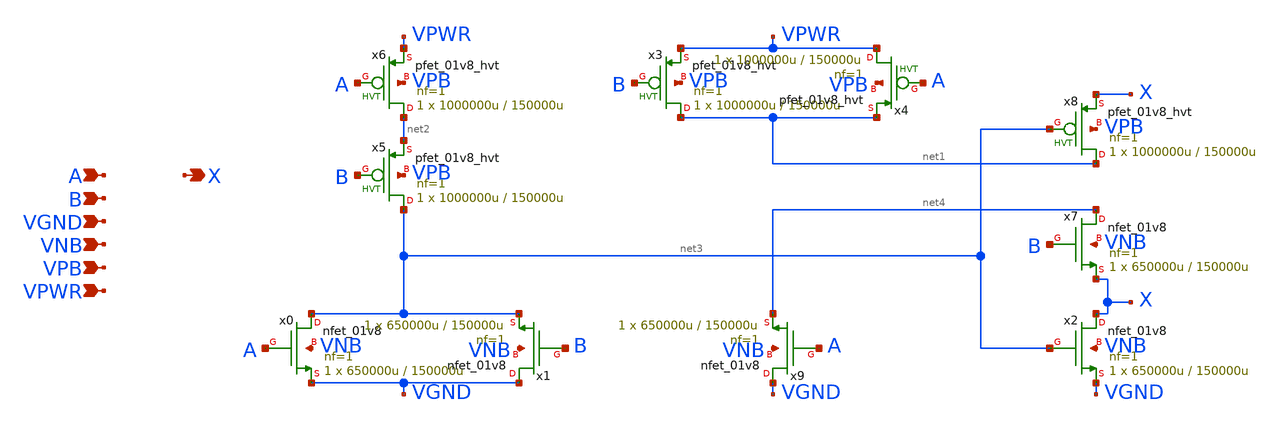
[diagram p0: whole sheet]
** sch_path: schematics/xor2/sky130_fd_sc_hd__xor2_1.sch
**.subckt sky130_fd_sc_hd__xor2_1 A X B VGND VNB VPB VPWR
*.ipin A
*.opin X
*.ipin B
*.ipin VGND
*.ipin VNB
*.ipin VPB
*.ipin VPWR
Xx3 net1 B VPWR VPB sky130_fd_pr__pfet_01v8_hvt L=150000u W=1000000u nf=1 ad='int((1 + 1)/2) * 1000000u / 1 * 0.29'
+ as='int((1 + 2)/2) * 1000000u / 1 * 0.29' pd='2*int((1 + 1)/2) * (1000000u / 1 + 0.29)' ps='2*int((1 + 2)/2) * (1000000u / 1 + 0.29)'
+ nrd='0.29 / 1000000u ' nrs='0.29 / 1000000u ' sa=0 sb=0 sd=0 mult=1 m=1
Xx4 VPWR A net1 VPB sky130_fd_pr__pfet_01v8_hvt L=150000u W=1000000u nf=1 ad='int((1 + 1)/2) * 1000000u / 1 * 0.29'
+ as='int((1 + 2)/2) * 1000000u / 1 * 0.29' pd='2*int((1 + 1)/2) * (1000000u / 1 + 0.29)' ps='2*int((1 + 2)/2) * (1000000u / 1 + 0.29)'
+ nrd='0.29 / 1000000u ' nrs='0.29 / 1000000u ' sa=0 sb=0 sd=0 mult=1 m=1
Xx6 net2 A VPWR VPB sky130_fd_pr__pfet_01v8_hvt L=150000u W=1000000u nf=1 ad='int((1 + 1)/2) * 1000000u / 1 * 0.29'
+ as='int((1 + 2)/2) * 1000000u / 1 * 0.29' pd='2*int((1 + 1)/2) * (1000000u / 1 + 0.29)' ps='2*int((1 + 2)/2) * (1000000u / 1 + 0.29)'
+ nrd='0.29 / 1000000u ' nrs='0.29 / 1000000u ' sa=0 sb=0 sd=0 mult=1 m=1
Xx5 net3 B net2 VPB sky130_fd_pr__pfet_01v8_hvt L=150000u W=1000000u nf=1 ad='int((1 + 1)/2) * 1000000u / 1 * 0.29'
+ as='int((1 + 2)/2) * 1000000u / 1 * 0.29' pd='2*int((1 + 1)/2) * (1000000u / 1 + 0.29)' ps='2*int((1 + 2)/2) * (1000000u / 1 + 0.29)'
+ nrd='0.29 / 1000000u ' nrs='0.29 / 1000000u ' sa=0 sb=0 sd=0 mult=1 m=1
Xx8 net1 net3 X VPB sky130_fd_pr__pfet_01v8_hvt L=150000u W=1000000u nf=1 ad='int((1 + 1)/2) * 1000000u / 1 * 0.29'
+ as='int((1 + 2)/2) * 1000000u / 1 * 0.29' pd='2*int((1 + 1)/2) * (1000000u / 1 + 0.29)' ps='2*int((1 + 2)/2) * (1000000u / 1 + 0.29)'
+ nrd='0.29 / 1000000u ' nrs='0.29 / 1000000u ' sa=0 sb=0 sd=0 mult=1 m=1
Xx0 net3 A VGND VNB sky130_fd_pr__nfet_01v8 L=150000u W=650000u nf=1 ad='int((1 + 1)/2) * 650000u / 1 * 0.29'
+ as='int((1 + 2)/2) * 650000u / 1 * 0.29' pd='2*int((1 + 1)/2) * (650000u / 1 + 0.29)' ps='2*int((1 + 2)/2) * (650000u / 1 + 0.29)'
+ nrd='0.29 / 650000u ' nrs='0.29 / 650000u ' sa=0 sb=0 sd=0 mult=1 m=1
Xx1 VGND B net3 VNB sky130_fd_pr__nfet_01v8 L=150000u W=650000u nf=1 ad='int((1 + 1)/2) * 650000u / 1 * 0.29'
+ as='int((1 + 2)/2) * 650000u / 1 * 0.29' pd='2*int((1 + 1)/2) * (650000u / 1 + 0.29)' ps='2*int((1 + 2)/2) * (650000u / 1 + 0.29)'
+ nrd='0.29 / 650000u ' nrs='0.29 / 650000u ' sa=0 sb=0 sd=0 mult=1 m=1
Xx2 X net3 VGND VNB sky130_fd_pr__nfet_01v8 L=150000u W=650000u nf=1 ad='int((1 + 1)/2) * 650000u / 1 * 0.29'
+ as='int((1 + 2)/2) * 650000u / 1 * 0.29' pd='2*int((1 + 1)/2) * (650000u / 1 + 0.29)' ps='2*int((1 + 2)/2) * (650000u / 1 + 0.29)'
+ nrd='0.29 / 650000u ' nrs='0.29 / 650000u ' sa=0 sb=0 sd=0 mult=1 m=1
Xx7 net4 B X VNB sky130_fd_pr__nfet_01v8 L=150000u W=650000u nf=1 ad='int((1 + 1)/2) * 650000u / 1 * 0.29'
+ as='int((1 + 2)/2) * 650000u / 1 * 0.29' pd='2*int((1 + 1)/2) * (650000u / 1 + 0.29)' ps='2*int((1 + 2)/2) * (650000u / 1 + 0.29)'
+ nrd='0.29 / 650000u ' nrs='0.29 / 650000u ' sa=0 sb=0 sd=0 mult=1 m=1
Xx9 VGND A net4 VNB sky130_fd_pr__nfet_01v8 L=150000u W=650000u nf=1 ad='int((1 + 1)/2) * 650000u / 1 * 0.29'
+ as='int((1 + 2)/2) * 650000u / 1 * 0.29' pd='2*int((1 + 1)/2) * (650000u / 1 + 0.29)' ps='2*int((1 + 2)/2) * (650000u / 1 + 0.29)'
+ nrd='0.29 / 650000u ' nrs='0.29 / 650000u ' sa=0 sb=0 sd=0 mult=1 m=1
**.ends
.end
